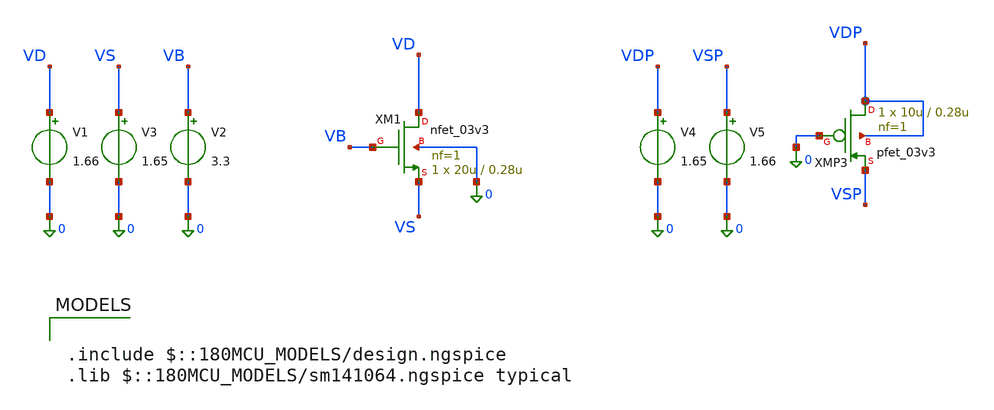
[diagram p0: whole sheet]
** sch_path: designs/sar_adc/samplehold/tb_resistencia/xschem/tb_resistencia.sch
**.subckt tb_resistencia
XM1 VD VB VS 0 nfet_03v3 L=0.28u W=20u nf=1 ad='int((nf+1)/2) * W/nf * 0.18u' as='int((nf+2)/2) * W/nf * 0.18u'
+ pd='2*int((nf+1)/2) * (W/nf + 0.18u)' ps='2*int((nf+2)/2) * (W/nf + 0.18u)' nrd='0.18u / W' nrs='0.18u / W'
+ sa=0 sb=0 sd=0 m=1
V1 VD 0 1.66
V2 VB 0 3.3
V3 VS 0 1.65
XMP3 VDP 0 VSP VDP pfet_03v3 L=0.28u W=10u nf=1 ad='int((nf+1)/2) * W/nf * 0.18u' as='int((nf+2)/2) * W/nf * 0.18u'
+ pd='2*int((nf+1)/2) * (W/nf + 0.18u)' ps='2*int((nf+2)/2) * (W/nf + 0.18u)' nrd='0.18u / W' nrs='0.18u / W'
+ sa=0 sb=0 sd=0 m=1
V4 VDP 0 1.65
V5 VSP 0 1.66
**** begin user architecture code

.include $::180MCU_MODELS/design.ngspice
.lib $::180MCU_MODELS/sm141064.ngspice typical





.control
  save all
  tran 0.1n 20u
  %plot (vd-vs)/i(v3)
  %plot vd-vs
  let resn=mean ((vd-vs)/i(v3))
  let resp=mean ((vdp-vsp)/i(v5))
 print resp
print resn
.endc



**** end user architecture code
**.ends
.end
